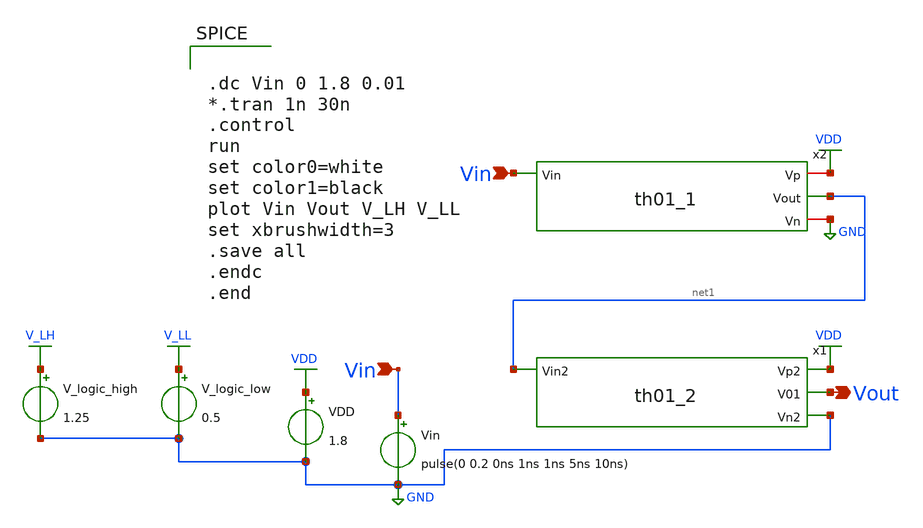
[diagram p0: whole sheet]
** sch_path: xschem/Vth_sch/Pre_layout/th01.sch
**.subckt th01 Vin Vout Vin
*.ipin Vin
*.opin Vout
*.ipin Vin
VDD VDD GND 1.8
Vin Vin GND pulse(0 0.2 0ns 1ns 1ns 5ns 10ns)
V_logic_high V_LH GND 1.25
V_logic_low V_LL GND 0.5
x2 VDD Vin net1 GND th01_1
x1 VDD net1 Vout GND th01_2
**** begin user architecture code


.lib /usr/local/share/pdk/sky130A/libs.tech/ngspice/sky130.lib.spice tt

.save all





.dc Vin 0 1.8 0.01
*.tran 1n 30n
.control
run
set color0=white
set color1=black
plot Vin Vout V_LH V_LL
set xbrushwidth=3
.save all
.endc
.end


**** end user architecture code
**.ends

* expanding   symbol:  /home/exotic/Desktop/ASIC_ADC/xschem/Vth_sch/Symbol/th01_1.sym # of pins=4
** sym_path: xschem/Vth_sch/Symbol/th01_1.sym
** sch_path: xschem/Vth_sch/Symbol/th01_1.sch
.subckt th01_1 Vp Vin Vout Vn
*.ipin Vin
*.opin Vout
*.iopin Vp
*.iopin Vn
XM5 Vout net1 Vp Vp sky130_fd_pr__pfet_01v8 L=0.15 W=2.5 nf=1 ad='int((nf+1)/2) * W/nf * 0.29' as='int((nf+2)/2) * W/nf * 0.29'
+ pd='2*int((nf+1)/2) * (W/nf + 0.29)' ps='2*int((nf+2)/2) * (W/nf + 0.29)' nrd='0.29 / W' nrs='0.29 / W'
+ sa=0 sb=0 sd=0 mult=1 m=1
XM4 Vout net1 Vn Vn sky130_fd_pr__nfet_01v8 L=0.80 W=0.48 nf=1 ad='int((nf+1)/2) * W/nf * 0.29' as='int((nf+2)/2) * W/nf * 0.29'
+ pd='2*int((nf+1)/2) * (W/nf + 0.29)' ps='2*int((nf+2)/2) * (W/nf + 0.29)' nrd='0.29 / W' nrs='0.29 / W'
+ sa=0 sb=0 sd=0 mult=1 m=1
XM2 net1 Vin Vp Vp sky130_fd_pr__pfet_01v8 L=1.00 W=0.55 nf=4 ad='int((nf+1)/2) * W/nf * 0.29' as='int((nf+2)/2) * W/nf * 0.29'
+ pd='2*int((nf+1)/2) * (W/nf + 0.29)' ps='2*int((nf+2)/2) * (W/nf + 0.29)' nrd='0.29 / W' nrs='0.29 / W'
+ sa=0 sb=0 sd=0 mult=1 m=1
XM3 net1 Vin Vn Vn sky130_fd_pr__nfet_01v8 L=0.15 W=3.5 nf=1 ad='int((nf+1)/2) * W/nf * 0.29' as='int((nf+2)/2) * W/nf * 0.29'
+ pd='2*int((nf+1)/2) * (W/nf + 0.29)' ps='2*int((nf+2)/2) * (W/nf + 0.29)' nrd='0.29 / W' nrs='0.29 / W'
+ sa=0 sb=0 sd=0 mult=1 m=1
.ends


* expanding   symbol:  /home/exotic/Desktop/ASIC_ADC/xschem/Vth_sch/Symbol/th01_2.sym # of pins=4
** sym_path: xschem/Vth_sch/Symbol/th01_2.sym
** sch_path: xschem/Vth_sch/Symbol/th01_2.sch
.subckt th01_2 Vp2 Vin2 V01 Vn2
*.opin Vn2
*.opin Vp2
*.ipin Vin2
*.opin V01
XM7 V01 net1 Vp2 Vp2 sky130_fd_pr__pfet_01v8 L=0.4700 W=0.42 nf=1 ad='int((nf+1)/2) * W/nf * 0.29' as='int((nf+2)/2) * W/nf * 0.29'
+ pd='2*int((nf+1)/2) * (W/nf + 0.29)' ps='2*int((nf+2)/2) * (W/nf + 0.29)' nrd='0.29 / W' nrs='0.29 / W'
+ sa=0 sb=0 sd=0 mult=1 m=1
XM6 V01 net1 Vn2 Vn2 sky130_fd_pr__nfet_01v8 L=0.15 W=0.47000 nf=1 ad='int((nf+1)/2) * W/nf * 0.29' as='int((nf+2)/2) * W/nf * 0.29'
+ pd='2*int((nf+1)/2) * (W/nf + 0.29)' ps='2*int((nf+2)/2) * (W/nf + 0.29)' nrd='0.29 / W' nrs='0.29 / W'
+ sa=0 sb=0 sd=0 mult=1 m=1
XM4 net1 Vin2 Vp2 Vp2 sky130_fd_pr__pfet_01v8 L=0.163000 W=0.42 nf=1 ad='int((nf+1)/2) * W/nf * 0.29'
+ as='int((nf+2)/2) * W/nf * 0.29' pd='2*int((nf+1)/2) * (W/nf + 0.29)' ps='2*int((nf+2)/2) * (W/nf + 0.29)'
+ nrd='0.29 / W' nrs='0.29 / W' sa=0 sb=0 sd=0 mult=1 m=1
XM5 net1 Vin2 Vn2 Vn2 sky130_fd_pr__nfet_01v8 L=0.163000 W=0.36 nf=1 ad='int((nf+1)/2) * W/nf * 0.29'
+ as='int((nf+2)/2) * W/nf * 0.29' pd='2*int((nf+1)/2) * (W/nf + 0.29)' ps='2*int((nf+2)/2) * (W/nf + 0.29)'
+ nrd='0.29 / W' nrs='0.29 / W' sa=0 sb=0 sd=0 mult=1 m=1
.ends

.GLOBAL VDD
.GLOBAL GND
.GLOBAL V_LH
.GLOBAL V_LL
.end
